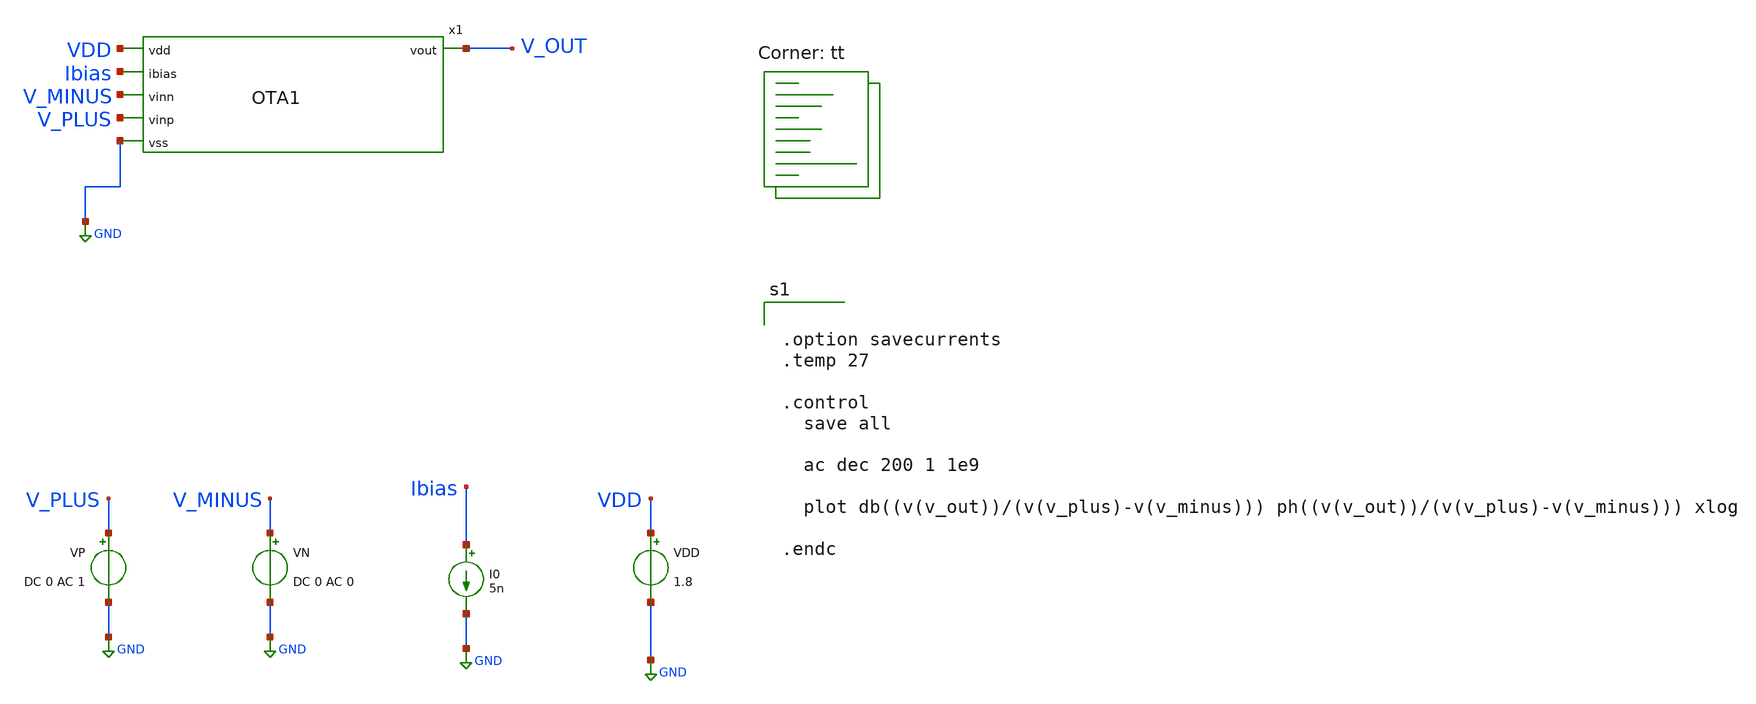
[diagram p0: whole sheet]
** sch_path: Schematic/OTA_AC_tb1.sch
**.subckt OTA_AC_tb1
VDD VDD GND 1.8
VP V_PLUS GND DC 0 AC 1
VN V_MINUS GND DC 0 AC 0
I0 Ibias GND 5n
x1 VDD Ibias V_OUT V_MINUS V_PLUS GND OTA1
**** begin user architecture code


.option savecurrents
.temp 27

.control
  save all

  ac dec 200 1 1e9

  plot db((v(v_out))/(v(v_plus)-v(v_minus))) ph((v(v_out))/(v(v_plus)-v(v_minus))) xlog

.endc



.lib $::SKYWATER_MODELS/sky130.lib.spice tt
**** end user architecture code
**.ends

* expanding   symbol:  /foss/designs/Analog_to_Spike/Schematic/OTA1.sym # of pins=6
** sym_path: Schematic/OTA1.sym
** sch_path: Schematic/OTA1.sch
.subckt OTA1 vdd ibias vout vinn vinp vss
*.ipin vdd
*.ipin vinp
*.ipin vinn
*.ipin vss
*.opin vout
*.ipin ibias
XM1 net1 vinp net3 vdd sky130_fd_pr__pfet_01v8 L=4.0 W=240 nf=1 ad='int((1 + 1)/2) * 240 / 1 * 0.29'
+ as='int((1 + 2)/2) * 240 / 1 * 0.29' pd='2*int((1 + 1)/2) * (240 / 1 + 0.29)' ps='2*int((1 + 2)/2) * (240 / 1 + 0.29)'
+ nrd='0.29 / 240 ' nrs='0.29 / 240 ' sa=0 sb=0 sd=0 mult=1 m=1
XM3 net1 net1 net6 vss sky130_fd_pr__nfet_01v8 L=20 W=2.24 nf=1 ad='int((1 + 1)/2) * 2.24 / 1 * 0.29'
+ as='int((1 + 2)/2) * 2.24 / 1 * 0.29' pd='2*int((1 + 1)/2) * (2.24 / 1 + 0.29)' ps='2*int((1 + 2)/2) * (2.24 / 1 + 0.29)'
+ nrd='0.29 / 2.24 ' nrs='0.29 / 2.24 ' sa=0 sb=0 sd=0 mult=1 m=1
XM4 net2 net2 net5 vss sky130_fd_pr__nfet_01v8 L=20 W=2.24 nf=1 ad='int((1 + 1)/2) * 2.24 / 1 * 0.29'
+ as='int((1 + 2)/2) * 2.24 / 1 * 0.29' pd='2*int((1 + 1)/2) * (2.24 / 1 + 0.29)' ps='2*int((1 + 2)/2) * (2.24 / 1 + 0.29)'
+ nrd='0.29 / 2.24 ' nrs='0.29 / 2.24 ' sa=0 sb=0 sd=0 mult=1 m=1
XM2 net2 vinn net3 vdd sky130_fd_pr__pfet_01v8 L=4.0 W=240 nf=1 ad='int((1 + 1)/2) * 240 / 1 * 0.29'
+ as='int((1 + 2)/2) * 240 / 1 * 0.29' pd='2*int((1 + 1)/2) * (240 / 1 + 0.29)' ps='2*int((1 + 2)/2) * (240 / 1 + 0.29)'
+ nrd='0.29 / 240 ' nrs='0.29 / 240 ' sa=0 sb=0 sd=0 mult=1 m=1
XM5 net4 net1 net8 vss sky130_fd_pr__nfet_01v8 L=20 W=2.24 nf=1 ad='int((1 + 1)/2) * 2.24 / 1 * 0.29'
+ as='int((1 + 2)/2) * 2.24 / 1 * 0.29' pd='2*int((1 + 1)/2) * (2.24 / 1 + 0.29)' ps='2*int((1 + 2)/2) * (2.24 / 1 + 0.29)'
+ nrd='0.29 / 2.24 ' nrs='0.29 / 2.24 ' sa=0 sb=0 sd=0 mult=1 m=1
XM6 vout net2 net7 vss sky130_fd_pr__nfet_01v8 L=20 W=2.24 nf=1 ad='int((1 + 1)/2) * 2.24 / 1 * 0.29'
+ as='int((1 + 2)/2) * 2.24 / 1 * 0.29' pd='2*int((1 + 1)/2) * (2.24 / 1 + 0.29)' ps='2*int((1 + 2)/2) * (2.24 / 1 + 0.29)'
+ nrd='0.29 / 2.24 ' nrs='0.29 / 2.24 ' sa=0 sb=0 sd=0 mult=1 m=1
XM8 vout net4 vdd vdd sky130_fd_pr__pfet_01v8 L=20 W=4 nf=1 ad='int((1 + 1)/2) * 4 / 1 * 0.29' as='int((1 + 2)/2) * 4 / 1 * 0.29'
+ pd='2*int((1 + 1)/2) * (4 / 1 + 0.29)' ps='2*int((1 + 2)/2) * (4 / 1 + 0.29)' nrd='0.29 / 4 ' nrs='0.29 / 4 '
+ sa=0 sb=0 sd=0 mult=1 m=1
XM9 ibias ibias vdd vdd sky130_fd_pr__pfet_01v8 L=10 W=10 nf=1 ad='int((1 + 1)/2) * 10 / 1 * 0.29' as='int((1 + 2)/2) * 10 / 1 * 0.29'
+ pd='2*int((1 + 1)/2) * (10 / 1 + 0.29)' ps='2*int((1 + 2)/2) * (10 / 1 + 0.29)' nrd='0.29 / 10 ' nrs='0.29 / 10 '
+ sa=0 sb=0 sd=0 mult=1 m=1
XM7 net4 net4 vdd vdd sky130_fd_pr__pfet_01v8 L=20 W=4 nf=1 ad='int((1 + 1)/2) * 4 / 1 * 0.29' as='int((1 + 2)/2) * 4 / 1 * 0.29'
+ pd='2*int((1 + 1)/2) * (4 / 1 + 0.29)' ps='2*int((1 + 2)/2) * (4 / 1 + 0.29)' nrd='0.29 / 4 ' nrs='0.29 / 4 '
+ sa=0 sb=0 sd=0 mult=1 m=1
XM10 net3 ibias vdd vdd sky130_fd_pr__pfet_01v8 L=10 W=10 nf=1 ad='int((1 + 1)/2) * 10 / 1 * 0.29' as='int((1 + 2)/2) * 10 / 1 * 0.29'
+ pd='2*int((1 + 1)/2) * (10 / 1 + 0.29)' ps='2*int((1 + 2)/2) * (10 / 1 + 0.29)' nrd='0.29 / 10 ' nrs='0.29 / 10 '
+ sa=0 sb=0 sd=0 mult=1 m=1
XM11 net6 net6 vss vss sky130_fd_pr__nfet_01v8 L=20 W=1.2 nf=1 ad='int((1 + 1)/2) * 1.2 / 1 * 0.29' as='int((1 + 2)/2) * 1.2 / 1 * 0.29'
+ pd='2*int((1 + 1)/2) * (1.2 / 1 + 0.29)' ps='2*int((1 + 2)/2) * (1.2 / 1 + 0.29)' nrd='0.29 / 1.2 ' nrs='0.29 / 1.2 '
+ sa=0 sb=0 sd=0 mult=1 m=1
XM12 net5 net5 vss vss sky130_fd_pr__nfet_01v8 L=20 W=1.2 nf=1 ad='int((1 + 1)/2) * 1.2 / 1 * 0.29' as='int((1 + 2)/2) * 1.2 / 1 * 0.29'
+ pd='2*int((1 + 1)/2) * (1.2 / 1 + 0.29)' ps='2*int((1 + 2)/2) * (1.2 / 1 + 0.29)' nrd='0.29 / 1.2 ' nrs='0.29 / 1.2 '
+ sa=0 sb=0 sd=0 mult=1 m=1
XM13 net8 net6 vss vss sky130_fd_pr__nfet_01v8 L=20 W=2.24 nf=1 ad='int((1 + 1)/2) * 2.24 / 1 * 0.29'
+ as='int((1 + 2)/2) * 2.24 / 1 * 0.29' pd='2*int((1 + 1)/2) * (2.24 / 1 + 0.29)' ps='2*int((1 + 2)/2) * (2.24 / 1 + 0.29)'
+ nrd='0.29 / 2.24 ' nrs='0.29 / 2.24 ' sa=0 sb=0 sd=0 mult=1 m=1
XM14 net7 net5 vss vss sky130_fd_pr__nfet_01v8 L=20 W=2.24 nf=1 ad='int((1 + 1)/2) * 2.24 / 1 * 0.29'
+ as='int((1 + 2)/2) * 2.24 / 1 * 0.29' pd='2*int((1 + 1)/2) * (2.24 / 1 + 0.29)' ps='2*int((1 + 2)/2) * (2.24 / 1 + 0.29)'
+ nrd='0.29 / 2.24 ' nrs='0.29 / 2.24 ' sa=0 sb=0 sd=0 mult=1 m=1
.ends

.GLOBAL GND
.end
